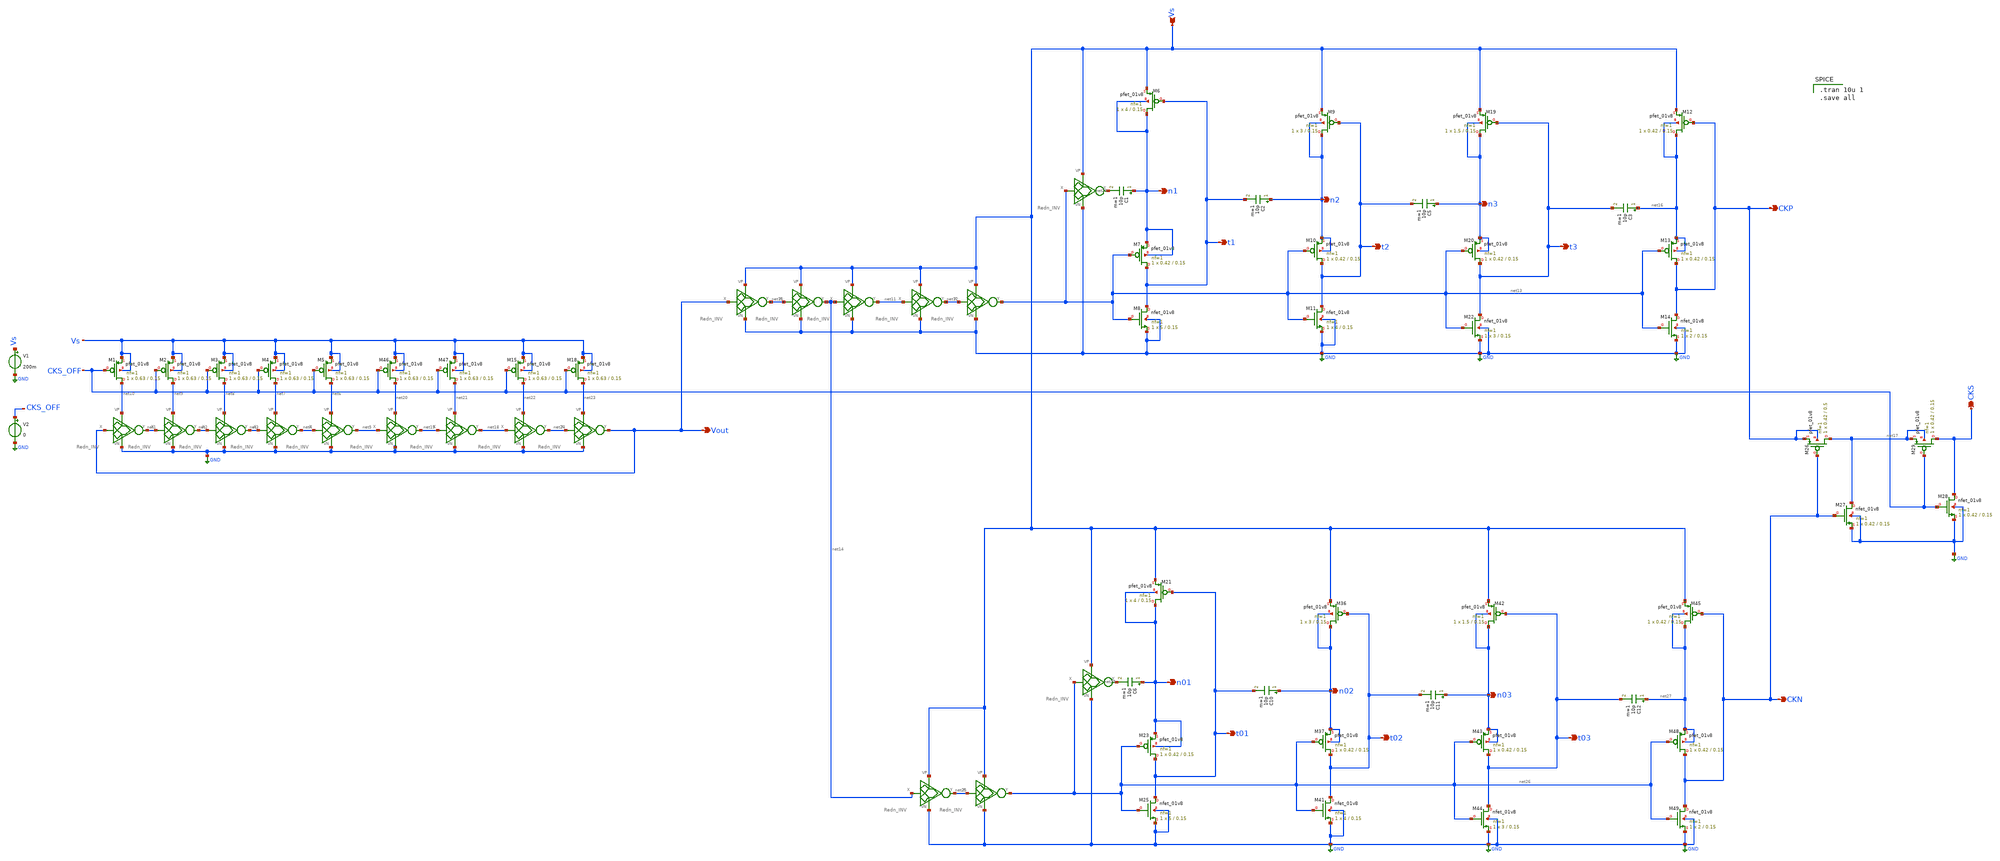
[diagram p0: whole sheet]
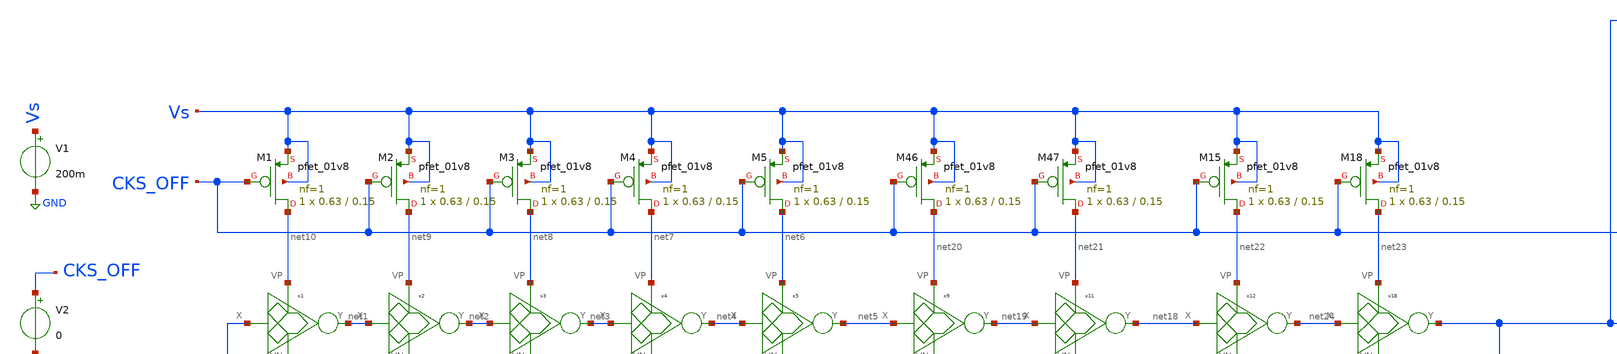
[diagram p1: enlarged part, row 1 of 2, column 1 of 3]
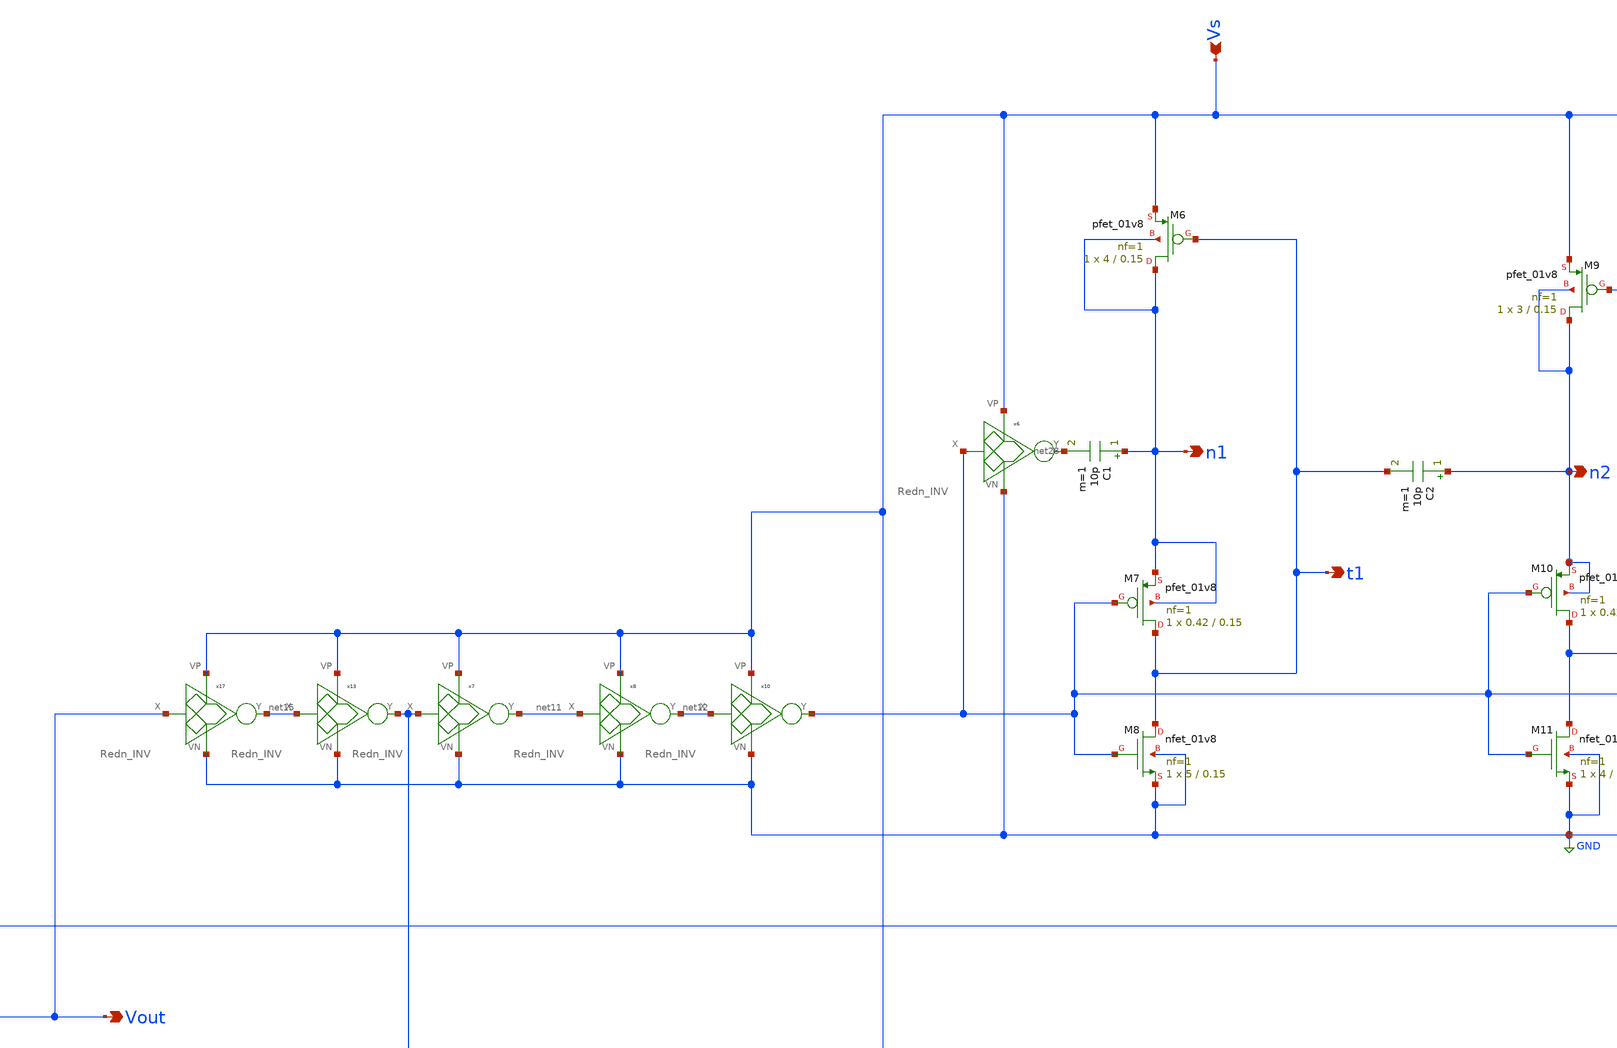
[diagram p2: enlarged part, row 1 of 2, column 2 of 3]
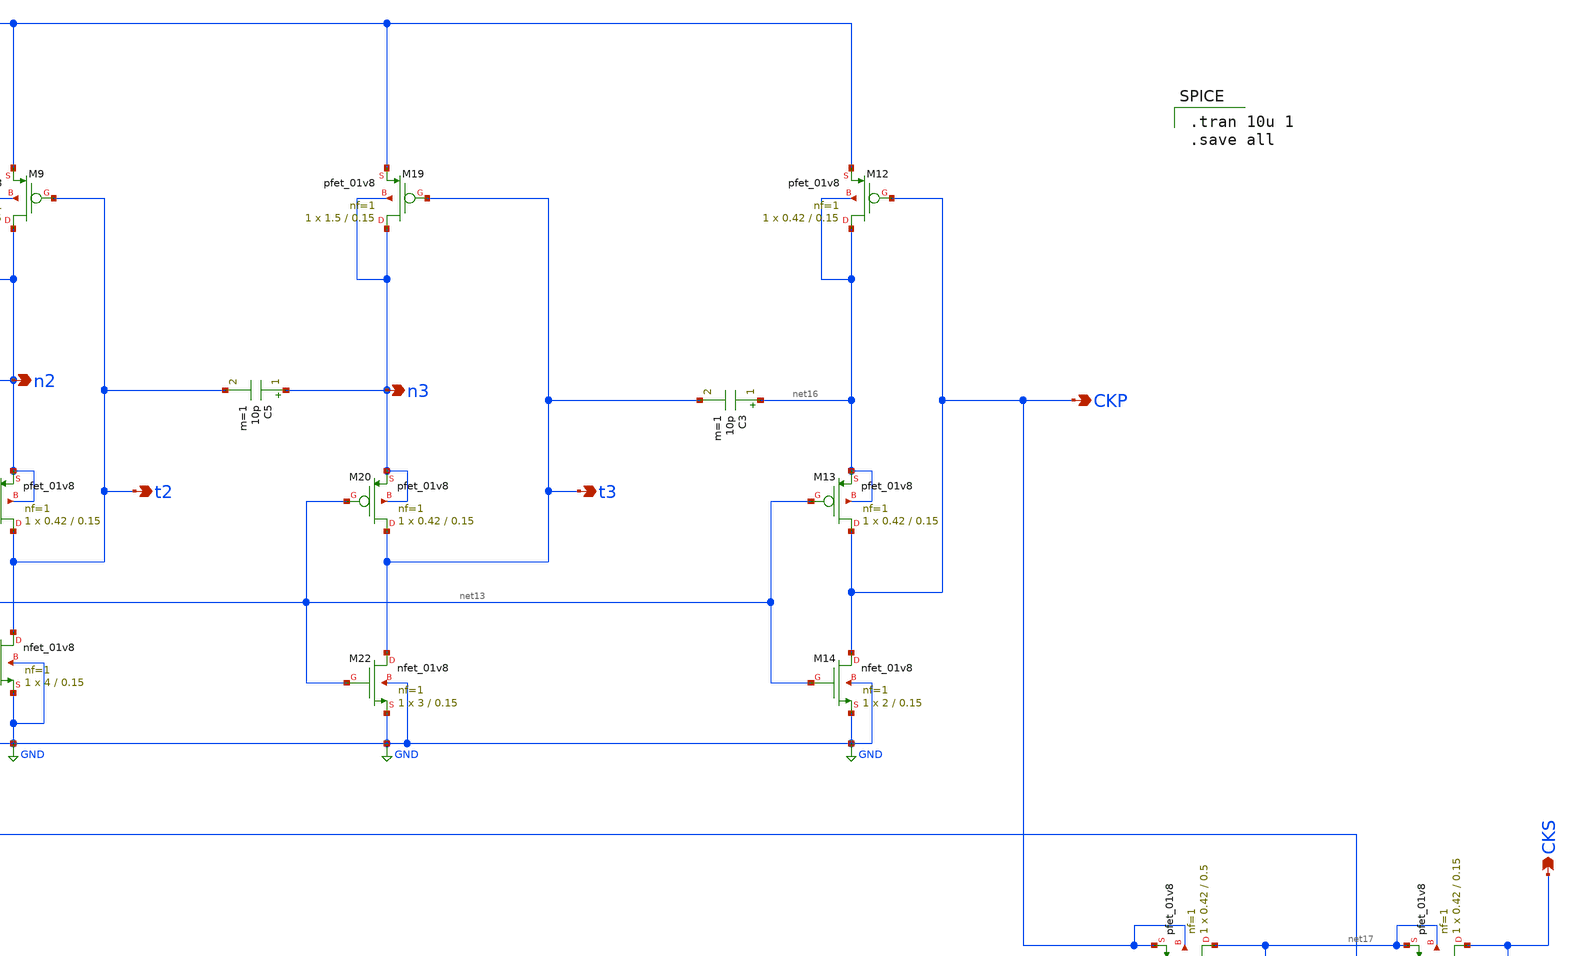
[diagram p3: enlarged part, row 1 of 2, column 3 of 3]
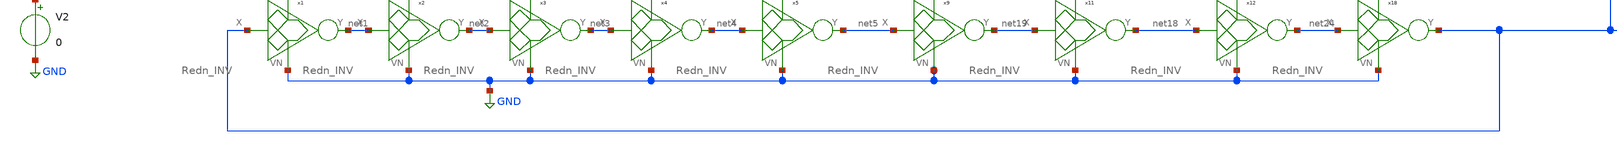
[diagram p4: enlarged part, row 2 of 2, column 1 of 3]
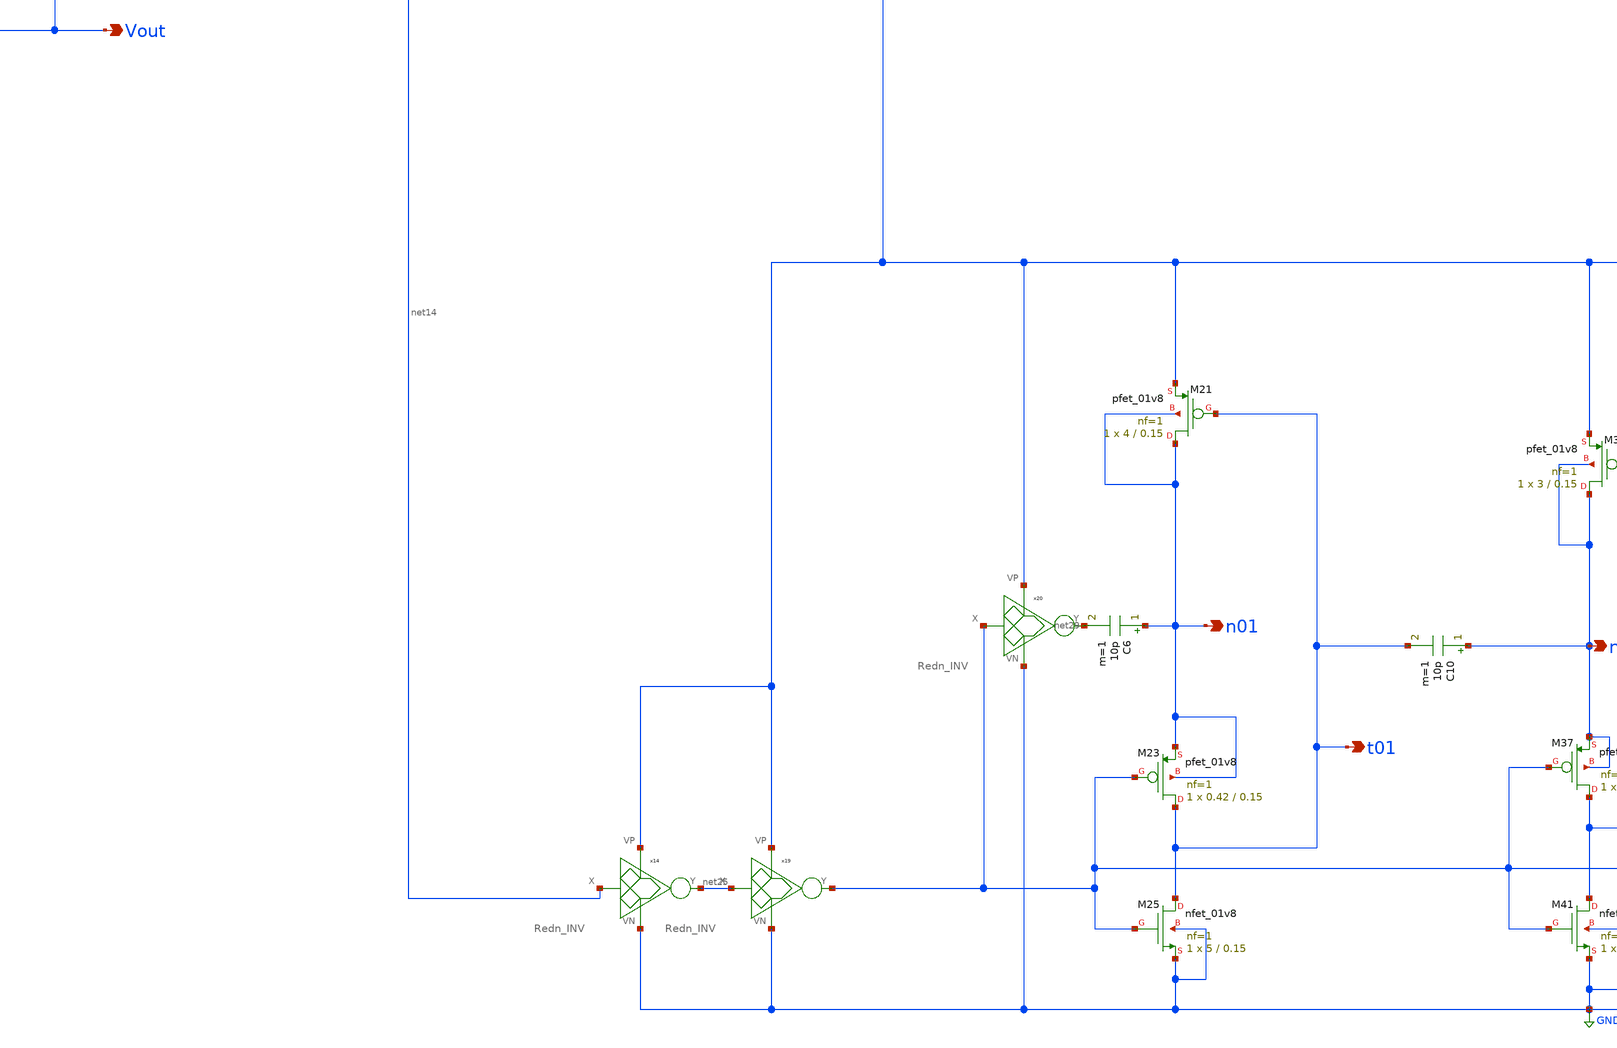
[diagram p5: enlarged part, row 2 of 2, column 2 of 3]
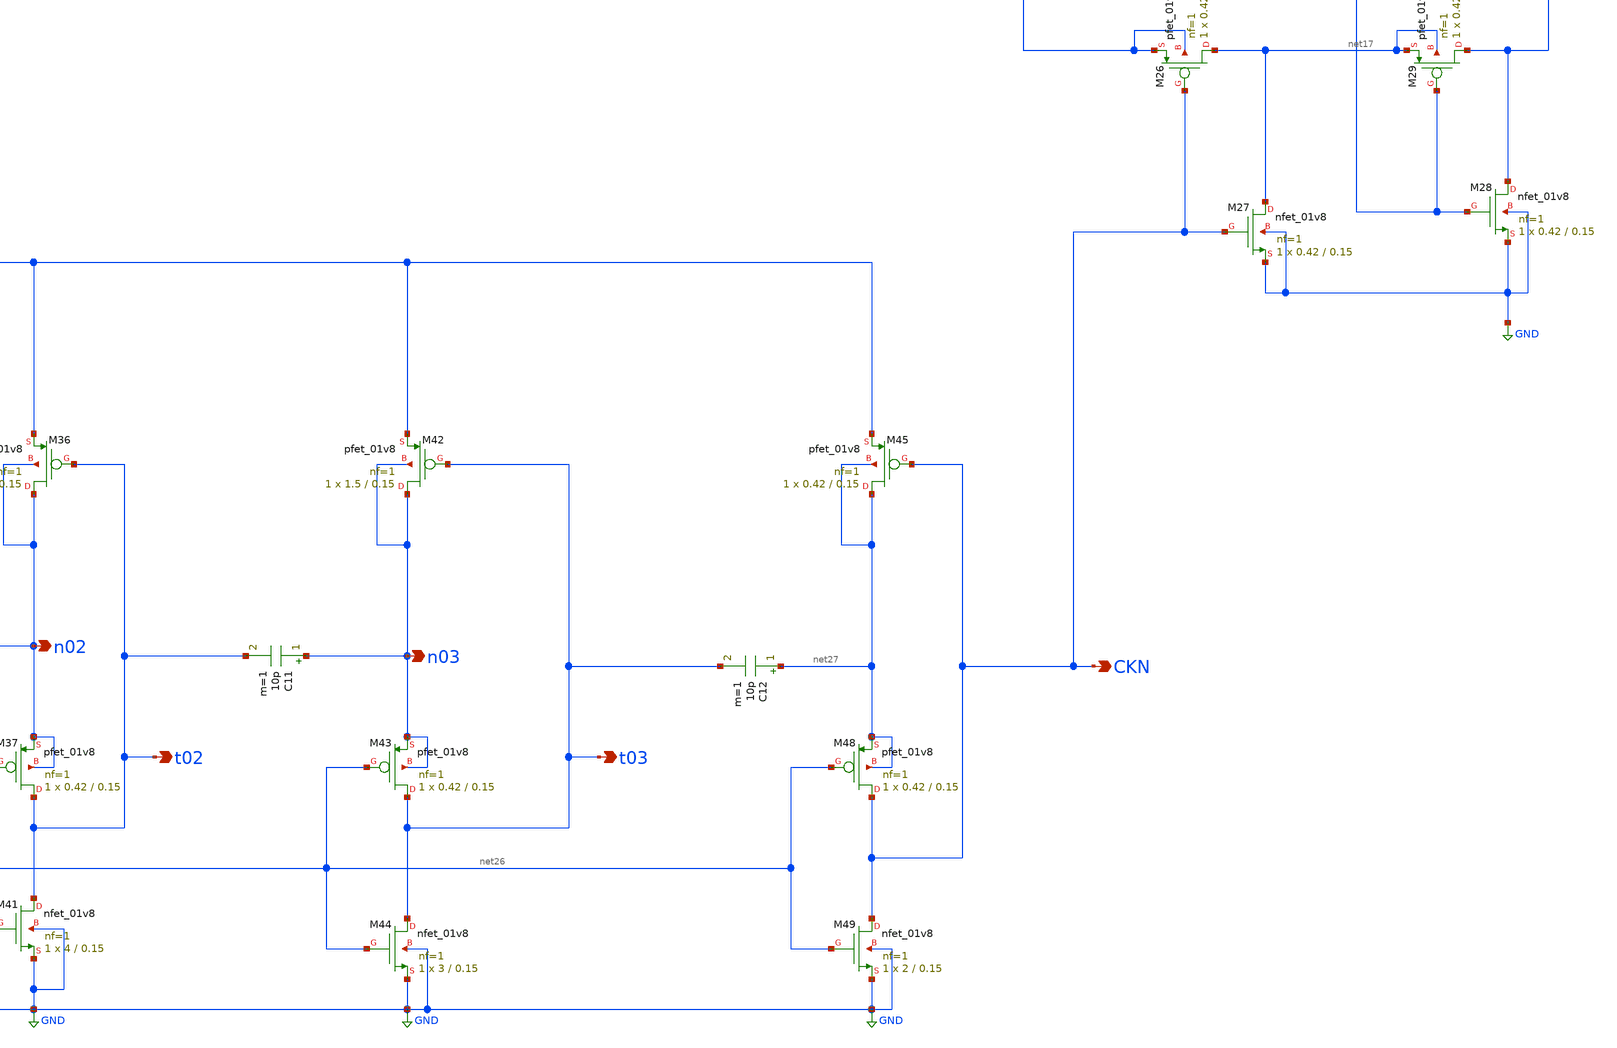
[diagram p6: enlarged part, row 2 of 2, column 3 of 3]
** sch_path: Blocks/Startup Converter/Startup_Conv_5.sch
**.subckt Startup_Conv_5 Vout Vs n1 t2 CKP CKS t3 t1 n2 n3 n01 t02 CKN t03 t01 n02 n03
*.opin Vout
*.ipin Vs
*.opin n1
*.opin t2
*.opin CKP
*.opin CKS
*.opin t3
*.opin t1
*.opin n2
*.opin n3
*.opin n01
*.opin t02
*.opin CKN
*.opin t03
*.opin t01
*.opin n02
*.opin n03
V1 Vs GND 200m
XM1 net10 CKS_OFF Vs Vs sky130_fd_pr__pfet_01v8 L=0.15 W=0.63 nf=1 ad='int((nf+1)/2) * W/nf * 0.29' as='int((nf+2)/2) * W/nf * 0.29'
+ pd='2*int((nf+1)/2) * (W/nf + 0.29)' ps='2*int((nf+2)/2) * (W/nf + 0.29)' nrd='0.29 / W' nrs='0.29 / W'
+ sa=0 sb=0 sd=0 mult=1 m=1
XM2 net9 CKS_OFF Vs Vs sky130_fd_pr__pfet_01v8 L=0.15 W=0.63 nf=1 ad='int((nf+1)/2) * W/nf * 0.29' as='int((nf+2)/2) * W/nf * 0.29'
+ pd='2*int((nf+1)/2) * (W/nf + 0.29)' ps='2*int((nf+2)/2) * (W/nf + 0.29)' nrd='0.29 / W' nrs='0.29 / W'
+ sa=0 sb=0 sd=0 mult=1 m=1
XM3 net8 CKS_OFF Vs Vs sky130_fd_pr__pfet_01v8 L=0.15 W=0.63 nf=1 ad='int((nf+1)/2) * W/nf * 0.29' as='int((nf+2)/2) * W/nf * 0.29'
+ pd='2*int((nf+1)/2) * (W/nf + 0.29)' ps='2*int((nf+2)/2) * (W/nf + 0.29)' nrd='0.29 / W' nrs='0.29 / W'
+ sa=0 sb=0 sd=0 mult=1 m=1
XM4 net7 CKS_OFF Vs Vs sky130_fd_pr__pfet_01v8 L=0.15 W=0.63 nf=1 ad='int((nf+1)/2) * W/nf * 0.29' as='int((nf+2)/2) * W/nf * 0.29'
+ pd='2*int((nf+1)/2) * (W/nf + 0.29)' ps='2*int((nf+2)/2) * (W/nf + 0.29)' nrd='0.29 / W' nrs='0.29 / W'
+ sa=0 sb=0 sd=0 mult=1 m=1
XM5 net6 CKS_OFF Vs Vs sky130_fd_pr__pfet_01v8 L=0.15 W=0.63 nf=1 ad='int((nf+1)/2) * W/nf * 0.29' as='int((nf+2)/2) * W/nf * 0.29'
+ pd='2*int((nf+1)/2) * (W/nf + 0.29)' ps='2*int((nf+2)/2) * (W/nf + 0.29)' nrd='0.29 / W' nrs='0.29 / W'
+ sa=0 sb=0 sd=0 mult=1 m=1
V2 CKS_OFF GND 0
x1 Vout net1 net10 GND Redn_INV
x2 net1 net2 net9 GND Redn_INV
x3 net2 net3 net8 GND Redn_INV
x4 net3 net4 net7 GND Redn_INV
x5 net4 net5 net6 GND Redn_INV
C1 n1 net28 10p m=1
XM6 n1 t1 Vs n1 sky130_fd_pr__pfet_01v8 L=0.15 W=4 nf=1 ad='int((nf+1)/2) * W/nf * 0.29' as='int((nf+2)/2) * W/nf * 0.29'
+ pd='2*int((nf+1)/2) * (W/nf + 0.29)' ps='2*int((nf+2)/2) * (W/nf + 0.29)' nrd='0.29 / W' nrs='0.29 / W'
+ sa=0 sb=0 sd=0 mult=1 m=1
XM7 t1 net13 n1 n1 sky130_fd_pr__pfet_01v8 L=0.15 W=0.42 nf=1 ad='int((nf+1)/2) * W/nf * 0.29' as='int((nf+2)/2) * W/nf * 0.29'
+ pd='2*int((nf+1)/2) * (W/nf + 0.29)' ps='2*int((nf+2)/2) * (W/nf + 0.29)' nrd='0.29 / W' nrs='0.29 / W'
+ sa=0 sb=0 sd=0 mult=1 m=1
XM8 t1 net13 GND GND sky130_fd_pr__nfet_01v8 L=0.15 W=5 nf=1 ad='int((nf+1)/2) * W/nf * 0.29' as='int((nf+2)/2) * W/nf * 0.29'
+ pd='2*int((nf+1)/2) * (W/nf + 0.29)' ps='2*int((nf+2)/2) * (W/nf + 0.29)' nrd='0.29 / W' nrs='0.29 / W'
+ sa=0 sb=0 sd=0 mult=1 m=1
XM9 n2 t2 Vs n2 sky130_fd_pr__pfet_01v8 L=0.15 W=3 nf=1 ad='int((nf+1)/2) * W/nf * 0.29' as='int((nf+2)/2) * W/nf * 0.29'
+ pd='2*int((nf+1)/2) * (W/nf + 0.29)' ps='2*int((nf+2)/2) * (W/nf + 0.29)' nrd='0.29 / W' nrs='0.29 / W'
+ sa=0 sb=0 sd=0 mult=1 m=1
XM10 t2 net13 n2 n2 sky130_fd_pr__pfet_01v8 L=0.15 W=0.42 nf=1 ad='int((nf+1)/2) * W/nf * 0.29' as='int((nf+2)/2) * W/nf * 0.29'
+ pd='2*int((nf+1)/2) * (W/nf + 0.29)' ps='2*int((nf+2)/2) * (W/nf + 0.29)' nrd='0.29 / W' nrs='0.29 / W'
+ sa=0 sb=0 sd=0 mult=1 m=1
XM11 t2 net13 GND GND sky130_fd_pr__nfet_01v8 L=0.15 W=4 nf=1 ad='int((nf+1)/2) * W/nf * 0.29' as='int((nf+2)/2) * W/nf * 0.29'
+ pd='2*int((nf+1)/2) * (W/nf + 0.29)' ps='2*int((nf+2)/2) * (W/nf + 0.29)' nrd='0.29 / W' nrs='0.29 / W'
+ sa=0 sb=0 sd=0 mult=1 m=1
C2 n2 t1 10p m=1
x7 net14 net11 Vs GND Redn_INV
x8 net11 net12 Vs GND Redn_INV
x10 net12 net13 Vs GND Redn_INV
x6 net13 net28 Vs GND Redn_INV
XM19 n3 t3 Vs n3 sky130_fd_pr__pfet_01v8 L=0.15 W=1.5 nf=1 ad='int((nf+1)/2) * W/nf * 0.29' as='int((nf+2)/2) * W/nf * 0.29'
+ pd='2*int((nf+1)/2) * (W/nf + 0.29)' ps='2*int((nf+2)/2) * (W/nf + 0.29)' nrd='0.29 / W' nrs='0.29 / W'
+ sa=0 sb=0 sd=0 mult=1 m=1
XM20 t3 net13 n3 n3 sky130_fd_pr__pfet_01v8 L=0.15 W=0.42 nf=1 ad='int((nf+1)/2) * W/nf * 0.29' as='int((nf+2)/2) * W/nf * 0.29'
+ pd='2*int((nf+1)/2) * (W/nf + 0.29)' ps='2*int((nf+2)/2) * (W/nf + 0.29)' nrd='0.29 / W' nrs='0.29 / W'
+ sa=0 sb=0 sd=0 mult=1 m=1
XM22 t3 net13 GND GND sky130_fd_pr__nfet_01v8 L=0.15 W=3 nf=1 ad='int((nf+1)/2) * W/nf * 0.29' as='int((nf+2)/2) * W/nf * 0.29'
+ pd='2*int((nf+1)/2) * (W/nf + 0.29)' ps='2*int((nf+2)/2) * (W/nf + 0.29)' nrd='0.29 / W' nrs='0.29 / W'
+ sa=0 sb=0 sd=0 mult=1 m=1
C5 n3 t2 10p m=1
x14 net14 net25 Vs GND Redn_INV
x13 net15 net14 Vs GND Redn_INV
x17 Vout net15 Vs GND Redn_INV
XM12 net16 CKP Vs net16 sky130_fd_pr__pfet_01v8 L=0.15 W=0.42 nf=1 ad='int((nf+1)/2) * W/nf * 0.29' as='int((nf+2)/2) * W/nf * 0.29'
+ pd='2*int((nf+1)/2) * (W/nf + 0.29)' ps='2*int((nf+2)/2) * (W/nf + 0.29)' nrd='0.29 / W' nrs='0.29 / W'
+ sa=0 sb=0 sd=0 mult=1 m=1
XM13 CKP net13 net16 net16 sky130_fd_pr__pfet_01v8 L=0.15 W=0.42 nf=1 ad='int((nf+1)/2) * W/nf * 0.29'
+ as='int((nf+2)/2) * W/nf * 0.29' pd='2*int((nf+1)/2) * (W/nf + 0.29)' ps='2*int((nf+2)/2) * (W/nf + 0.29)'
+ nrd='0.29 / W' nrs='0.29 / W' sa=0 sb=0 sd=0 mult=1 m=1
XM14 CKP net13 GND GND sky130_fd_pr__nfet_01v8 L=0.15 W=2 nf=1 ad='int((nf+1)/2) * W/nf * 0.29' as='int((nf+2)/2) * W/nf * 0.29'
+ pd='2*int((nf+1)/2) * (W/nf + 0.29)' ps='2*int((nf+2)/2) * (W/nf + 0.29)' nrd='0.29 / W' nrs='0.29 / W'
+ sa=0 sb=0 sd=0 mult=1 m=1
C3 net16 t3 10p m=1
XM26 net17 CKN CKP CKP sky130_fd_pr__pfet_01v8 L=0.5 W=0.42 nf=1 ad='int((nf+1)/2) * W/nf * 0.29' as='int((nf+2)/2) * W/nf * 0.29'
+ pd='2*int((nf+1)/2) * (W/nf + 0.29)' ps='2*int((nf+2)/2) * (W/nf + 0.29)' nrd='0.29 / W' nrs='0.29 / W'
+ sa=0 sb=0 sd=0 mult=1 m=1
XM27 net17 CKN GND GND sky130_fd_pr__nfet_01v8 L=0.15 W=0.42 nf=1 ad='int((nf+1)/2) * W/nf * 0.29' as='int((nf+2)/2) * W/nf * 0.29'
+ pd='2*int((nf+1)/2) * (W/nf + 0.29)' ps='2*int((nf+2)/2) * (W/nf + 0.29)' nrd='0.29 / W' nrs='0.29 / W'
+ sa=0 sb=0 sd=0 mult=1 m=1
XM28 CKS CKS_OFF GND GND sky130_fd_pr__nfet_01v8 L=0.15 W=0.42 nf=1 ad='int((nf+1)/2) * W/nf * 0.29'
+ as='int((nf+2)/2) * W/nf * 0.29' pd='2*int((nf+1)/2) * (W/nf + 0.29)' ps='2*int((nf+2)/2) * (W/nf + 0.29)'
+ nrd='0.29 / W' nrs='0.29 / W' sa=0 sb=0 sd=0 mult=1 m=1
XM29 CKS CKS_OFF net17 net17 sky130_fd_pr__pfet_01v8 L=0.15 W=0.42 nf=1 ad='int((nf+1)/2) * W/nf * 0.29'
+ as='int((nf+2)/2) * W/nf * 0.29' pd='2*int((nf+1)/2) * (W/nf + 0.29)' ps='2*int((nf+2)/2) * (W/nf + 0.29)'
+ nrd='0.29 / W' nrs='0.29 / W' sa=0 sb=0 sd=0 mult=1 m=1
x9 net5 net19 net20 GND Redn_INV
x11 net19 net18 net21 GND Redn_INV
XM46 net20 CKS_OFF Vs Vs sky130_fd_pr__pfet_01v8 L=0.15 W=0.63 nf=1 ad='int((nf+1)/2) * W/nf * 0.29'
+ as='int((nf+2)/2) * W/nf * 0.29' pd='2*int((nf+1)/2) * (W/nf + 0.29)' ps='2*int((nf+2)/2) * (W/nf + 0.29)'
+ nrd='0.29 / W' nrs='0.29 / W' sa=0 sb=0 sd=0 mult=1 m=1
XM47 net21 CKS_OFF Vs Vs sky130_fd_pr__pfet_01v8 L=0.15 W=0.63 nf=1 ad='int((nf+1)/2) * W/nf * 0.29'
+ as='int((nf+2)/2) * W/nf * 0.29' pd='2*int((nf+1)/2) * (W/nf + 0.29)' ps='2*int((nf+2)/2) * (W/nf + 0.29)'
+ nrd='0.29 / W' nrs='0.29 / W' sa=0 sb=0 sd=0 mult=1 m=1
x12 net18 net24 net22 GND Redn_INV
XM15 net22 CKS_OFF Vs Vs sky130_fd_pr__pfet_01v8 L=0.15 W=0.63 nf=1 ad='int((nf+1)/2) * W/nf * 0.29'
+ as='int((nf+2)/2) * W/nf * 0.29' pd='2*int((nf+1)/2) * (W/nf + 0.29)' ps='2*int((nf+2)/2) * (W/nf + 0.29)'
+ nrd='0.29 / W' nrs='0.29 / W' sa=0 sb=0 sd=0 mult=1 m=1
x18 net24 Vout net23 GND Redn_INV
XM18 net23 CKS_OFF Vs Vs sky130_fd_pr__pfet_01v8 L=0.15 W=0.63 nf=1 ad='int((nf+1)/2) * W/nf * 0.29'
+ as='int((nf+2)/2) * W/nf * 0.29' pd='2*int((nf+1)/2) * (W/nf + 0.29)' ps='2*int((nf+2)/2) * (W/nf + 0.29)'
+ nrd='0.29 / W' nrs='0.29 / W' sa=0 sb=0 sd=0 mult=1 m=1
C6 n01 net29 10p m=1
XM21 n01 t01 Vs n01 sky130_fd_pr__pfet_01v8 L=0.15 W=4 nf=1 ad='int((nf+1)/2) * W/nf * 0.29' as='int((nf+2)/2) * W/nf * 0.29'
+ pd='2*int((nf+1)/2) * (W/nf + 0.29)' ps='2*int((nf+2)/2) * (W/nf + 0.29)' nrd='0.29 / W' nrs='0.29 / W'
+ sa=0 sb=0 sd=0 mult=1 m=1
XM23 t01 net26 n01 n01 sky130_fd_pr__pfet_01v8 L=0.15 W=0.42 nf=1 ad='int((nf+1)/2) * W/nf * 0.29' as='int((nf+2)/2) * W/nf * 0.29'
+ pd='2*int((nf+1)/2) * (W/nf + 0.29)' ps='2*int((nf+2)/2) * (W/nf + 0.29)' nrd='0.29 / W' nrs='0.29 / W'
+ sa=0 sb=0 sd=0 mult=1 m=1
XM25 t01 net26 GND GND sky130_fd_pr__nfet_01v8 L=0.15 W=5 nf=1 ad='int((nf+1)/2) * W/nf * 0.29' as='int((nf+2)/2) * W/nf * 0.29'
+ pd='2*int((nf+1)/2) * (W/nf + 0.29)' ps='2*int((nf+2)/2) * (W/nf + 0.29)' nrd='0.29 / W' nrs='0.29 / W'
+ sa=0 sb=0 sd=0 mult=1 m=1
XM36 n02 t02 Vs n02 sky130_fd_pr__pfet_01v8 L=0.15 W=3 nf=1 ad='int((nf+1)/2) * W/nf * 0.29' as='int((nf+2)/2) * W/nf * 0.29'
+ pd='2*int((nf+1)/2) * (W/nf + 0.29)' ps='2*int((nf+2)/2) * (W/nf + 0.29)' nrd='0.29 / W' nrs='0.29 / W'
+ sa=0 sb=0 sd=0 mult=1 m=1
XM37 t02 net26 n02 n02 sky130_fd_pr__pfet_01v8 L=0.15 W=0.42 nf=1 ad='int((nf+1)/2) * W/nf * 0.29' as='int((nf+2)/2) * W/nf * 0.29'
+ pd='2*int((nf+1)/2) * (W/nf + 0.29)' ps='2*int((nf+2)/2) * (W/nf + 0.29)' nrd='0.29 / W' nrs='0.29 / W'
+ sa=0 sb=0 sd=0 mult=1 m=1
XM41 t02 net26 GND GND sky130_fd_pr__nfet_01v8 L=0.15 W=4 nf=1 ad='int((nf+1)/2) * W/nf * 0.29' as='int((nf+2)/2) * W/nf * 0.29'
+ pd='2*int((nf+1)/2) * (W/nf + 0.29)' ps='2*int((nf+2)/2) * (W/nf + 0.29)' nrd='0.29 / W' nrs='0.29 / W'
+ sa=0 sb=0 sd=0 mult=1 m=1
C10 n02 t01 10p m=1
x19 net25 net26 Vs GND Redn_INV
x20 net26 net29 Vs GND Redn_INV
XM42 n03 t03 Vs n03 sky130_fd_pr__pfet_01v8 L=0.15 W=1.5 nf=1 ad='int((nf+1)/2) * W/nf * 0.29' as='int((nf+2)/2) * W/nf * 0.29'
+ pd='2*int((nf+1)/2) * (W/nf + 0.29)' ps='2*int((nf+2)/2) * (W/nf + 0.29)' nrd='0.29 / W' nrs='0.29 / W'
+ sa=0 sb=0 sd=0 mult=1 m=1
XM43 t03 net26 n03 n03 sky130_fd_pr__pfet_01v8 L=0.15 W=0.42 nf=1 ad='int((nf+1)/2) * W/nf * 0.29' as='int((nf+2)/2) * W/nf * 0.29'
+ pd='2*int((nf+1)/2) * (W/nf + 0.29)' ps='2*int((nf+2)/2) * (W/nf + 0.29)' nrd='0.29 / W' nrs='0.29 / W'
+ sa=0 sb=0 sd=0 mult=1 m=1
XM44 t03 net26 GND GND sky130_fd_pr__nfet_01v8 L=0.15 W=3 nf=1 ad='int((nf+1)/2) * W/nf * 0.29' as='int((nf+2)/2) * W/nf * 0.29'
+ pd='2*int((nf+1)/2) * (W/nf + 0.29)' ps='2*int((nf+2)/2) * (W/nf + 0.29)' nrd='0.29 / W' nrs='0.29 / W'
+ sa=0 sb=0 sd=0 mult=1 m=1
C11 n03 t02 10p m=1
XM45 net27 CKN Vs net27 sky130_fd_pr__pfet_01v8 L=0.15 W=0.42 nf=1 ad='int((nf+1)/2) * W/nf * 0.29' as='int((nf+2)/2) * W/nf * 0.29'
+ pd='2*int((nf+1)/2) * (W/nf + 0.29)' ps='2*int((nf+2)/2) * (W/nf + 0.29)' nrd='0.29 / W' nrs='0.29 / W'
+ sa=0 sb=0 sd=0 mult=1 m=1
XM48 CKN net26 net27 net27 sky130_fd_pr__pfet_01v8 L=0.15 W=0.42 nf=1 ad='int((nf+1)/2) * W/nf * 0.29'
+ as='int((nf+2)/2) * W/nf * 0.29' pd='2*int((nf+1)/2) * (W/nf + 0.29)' ps='2*int((nf+2)/2) * (W/nf + 0.29)'
+ nrd='0.29 / W' nrs='0.29 / W' sa=0 sb=0 sd=0 mult=1 m=1
XM49 CKN net26 GND GND sky130_fd_pr__nfet_01v8 L=0.15 W=2 nf=1 ad='int((nf+1)/2) * W/nf * 0.29' as='int((nf+2)/2) * W/nf * 0.29'
+ pd='2*int((nf+1)/2) * (W/nf + 0.29)' ps='2*int((nf+2)/2) * (W/nf + 0.29)' nrd='0.29 / W' nrs='0.29 / W'
+ sa=0 sb=0 sd=0 mult=1 m=1
C12 net27 t03 10p m=1
**** begin user architecture code

** opencircuitdesign pdks install
.lib $::SKYWATER_MODELS/sky130.lib.spice tt



.tran 10u 1
.save all

**** end user architecture code
**.ends

* expanding   symbol:  component/Reduntant_Inverter/Redn_INV.sym # of pins=4
** sym_path: component/Reduntant_Inverter/Redn_INV.sym
** sch_path: component/Reduntant_Inverter/Redn_INV.sch
.subckt Redn_INV X Y VP VN
*.opin Y
*.ipin X
*.iopin VP
*.iopin VN
XM15 net4 X VN VN sky130_fd_pr__nfet_01v8_lvt L=0.15 W=1 nf=1 ad='int((nf+1)/2) * W/nf * 0.29' as='int((nf+2)/2) * W/nf * 0.29'
+ pd='2*int((nf+1)/2) * (W/nf + 0.29)' ps='2*int((nf+2)/2) * (W/nf + 0.29)' nrd='0.29 / W' nrs='0.29 / W'
+ sa=0 sb=0 sd=0 mult=1 m=1
XM1 net5 X net3 VN sky130_fd_pr__nfet_01v8_lvt L=0.15 W=3.25 nf=1 ad='int((nf+1)/2) * W/nf * 0.29' as='int((nf+2)/2) * W/nf * 0.29'
+ pd='2*int((nf+1)/2) * (W/nf + 0.29)' ps='2*int((nf+2)/2) * (W/nf + 0.29)' nrd='0.29 / W' nrs='0.29 / W'
+ sa=0 sb=0 sd=0 mult=1 m=1
XM16 Y X net6 VN sky130_fd_pr__nfet_01v8_lvt L=0.15 W=6.5 nf=1 ad='int((nf+1)/2) * W/nf * 0.29' as='int((nf+2)/2) * W/nf * 0.29'
+ pd='2*int((nf+1)/2) * (W/nf + 0.29)' ps='2*int((nf+2)/2) * (W/nf + 0.29)' nrd='0.29 / W' nrs='0.29 / W'
+ sa=0 sb=0 sd=0 mult=1 m=1
XM17 net3 X VN VN sky130_fd_pr__nfet_01v8_lvt L=0.15 W=3.25 nf=1 ad='int((nf+1)/2) * W/nf * 0.29' as='int((nf+2)/2) * W/nf * 0.29'
+ pd='2*int((nf+1)/2) * (W/nf + 0.29)' ps='2*int((nf+2)/2) * (W/nf + 0.29)' nrd='0.29 / W' nrs='0.29 / W'
+ sa=0 sb=0 sd=0 mult=1 m=1
XM18 net2 X VN VN sky130_fd_pr__nfet_01v8_lvt L=0.15 W=1.5 nf=1 ad='int((nf+1)/2) * W/nf * 0.29' as='int((nf+2)/2) * W/nf * 0.29'
+ pd='2*int((nf+1)/2) * (W/nf + 0.29)' ps='2*int((nf+2)/2) * (W/nf + 0.29)' nrd='0.29 / W' nrs='0.29 / W'
+ sa=0 sb=0 sd=0 mult=1 m=1
XM19 net1 X VN VN sky130_fd_pr__nfet_01v8_lvt L=0.15 W=6.5 nf=1 ad='int((nf+1)/2) * W/nf * 0.29' as='int((nf+2)/2) * W/nf * 0.29'
+ pd='2*int((nf+1)/2) * (W/nf + 0.29)' ps='2*int((nf+2)/2) * (W/nf + 0.29)' nrd='0.29 / W' nrs='0.29 / W'
+ sa=0 sb=0 sd=0 mult=1 m=1
XM20 net6 X net1 VN sky130_fd_pr__nfet_01v8_lvt L=0.15 W=6.5 nf=1 ad='int((nf+1)/2) * W/nf * 0.29' as='int((nf+2)/2) * W/nf * 0.29'
+ pd='2*int((nf+1)/2) * (W/nf + 0.29)' ps='2*int((nf+2)/2) * (W/nf + 0.29)' nrd='0.29 / W' nrs='0.29 / W'
+ sa=0 sb=0 sd=0 mult=1 m=1
XM2 net4 X VP VP sky130_fd_pr__pfet_01v8 L=0.15 W=10 nf=1 ad='int((nf+1)/2) * W/nf * 0.29' as='int((nf+2)/2) * W/nf * 0.29'
+ pd='2*int((nf+1)/2) * (W/nf + 0.29)' ps='2*int((nf+2)/2) * (W/nf + 0.29)' nrd='0.29 / W' nrs='0.29 / W'
+ sa=0 sb=0 sd=0 mult=1 m=1
XM5 net5 X net4 net4 sky130_fd_pr__pfet_01v8 L=0.15 W=10 nf=1 ad='int((nf+1)/2) * W/nf * 0.29' as='int((nf+2)/2) * W/nf * 0.29'
+ pd='2*int((nf+1)/2) * (W/nf + 0.29)' ps='2*int((nf+2)/2) * (W/nf + 0.29)' nrd='0.29 / W' nrs='0.29 / W'
+ sa=0 sb=0 sd=0 mult=1 m=1
XM6 Y X net5 VP sky130_fd_pr__pfet_01v8 L=0.15 W=10 nf=1 ad='int((nf+1)/2) * W/nf * 0.29' as='int((nf+2)/2) * W/nf * 0.29'
+ pd='2*int((nf+1)/2) * (W/nf + 0.29)' ps='2*int((nf+2)/2) * (W/nf + 0.29)' nrd='0.29 / W' nrs='0.29 / W'
+ sa=0 sb=0 sd=0 mult=1 m=1
XM8 net3 X VP VP sky130_fd_pr__pfet_01v8 L=0.15 W=2 nf=1 ad='int((nf+1)/2) * W/nf * 0.29' as='int((nf+2)/2) * W/nf * 0.29'
+ pd='2*int((nf+1)/2) * (W/nf + 0.29)' ps='2*int((nf+2)/2) * (W/nf + 0.29)' nrd='0.29 / W' nrs='0.29 / W'
+ sa=0 sb=0 sd=0 mult=1 m=1
XM12 net2 X VP VP sky130_fd_pr__pfet_01v8 L=0.15 W=5 nf=1 ad='int((nf+1)/2) * W/nf * 0.29' as='int((nf+2)/2) * W/nf * 0.29'
+ pd='2*int((nf+1)/2) * (W/nf + 0.29)' ps='2*int((nf+2)/2) * (W/nf + 0.29)' nrd='0.29 / W' nrs='0.29 / W'
+ sa=0 sb=0 sd=0 mult=1 m=1
XM14 net6 X net2 VP sky130_fd_pr__pfet_01v8 L=0.15 W=5 nf=1 ad='int((nf+1)/2) * W/nf * 0.29' as='int((nf+2)/2) * W/nf * 0.29'
+ pd='2*int((nf+1)/2) * (W/nf + 0.29)' ps='2*int((nf+2)/2) * (W/nf + 0.29)' nrd='0.29 / W' nrs='0.29 / W'
+ sa=0 sb=0 sd=0 mult=1 m=1
XM21 net1 X VP VP sky130_fd_pr__pfet_01v8 L=0.15 W=1.5 nf=1 ad='int((nf+1)/2) * W/nf * 0.29' as='int((nf+2)/2) * W/nf * 0.29'
+ pd='2*int((nf+1)/2) * (W/nf + 0.29)' ps='2*int((nf+2)/2) * (W/nf + 0.29)' nrd='0.29 / W' nrs='0.29 / W'
+ sa=0 sb=0 sd=0 mult=1 m=1
.ends

.GLOBAL GND
.end
